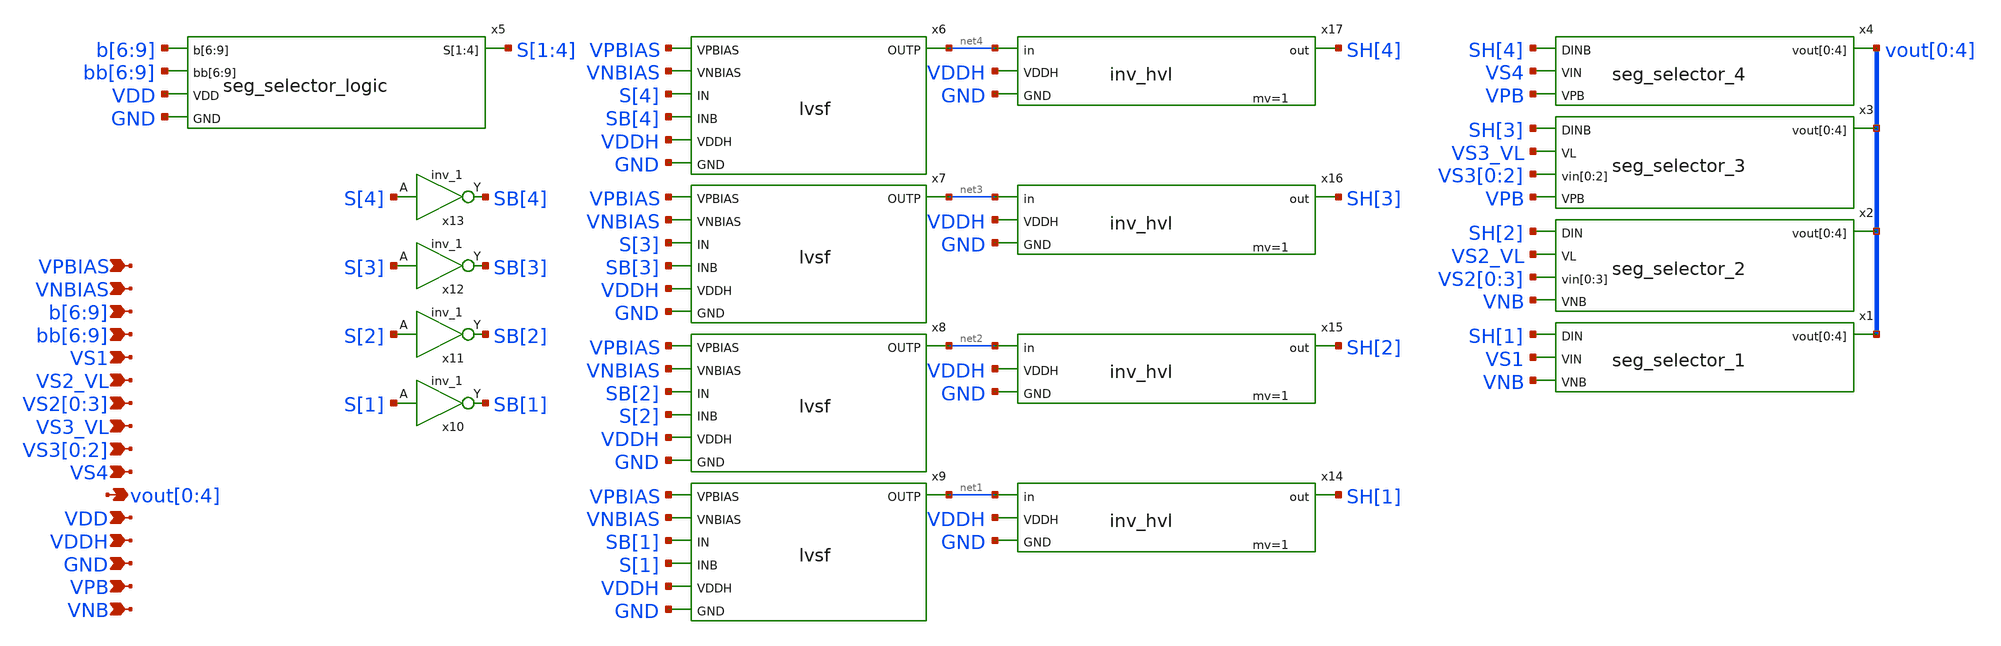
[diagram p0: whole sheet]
** sch_path: xschem/seg_selector.sch
**.subckt seg_selector vout[0],vout[1],vout[2],vout[3],vout[4] VNB VPB b[6],b[7],b[8],b[9] VS1
*+ VS2[0],VS2[1],VS2[2],VS2[3] VS3[0],VS3[1],VS3[2] VS4 bb[6],bb[7],bb[8],bb[9] GND VDD VPBIAS VNBIAS VDDH VS2_VL VS3_VL
*.opin vout[0],vout[1],vout[2],vout[3],vout[4]
*.ipin VNB
*.ipin VPB
*.ipin b[6],b[7],b[8],b[9]
*.ipin VS1
*.ipin VS2[0],VS2[1],VS2[2],VS2[3]
*.ipin VS3[0],VS3[1],VS3[2]
*.ipin VS4
*.ipin bb[6],bb[7],bb[8],bb[9]
*.ipin GND
*.ipin VDD
*.ipin VPBIAS
*.ipin VNBIAS
*.ipin VDDH
*.ipin VS2_VL
*.ipin VS3_VL
x1 SH[1] VS1 vout[0] vout[1] vout[2] vout[3] vout[4] VNB seg_selector_1
x2 SH[2] VS2_VL VS2[0] VS2[1] VS2[2] VS2[3] vout[0] vout[1] vout[2] vout[3] vout[4] VNB
+ seg_selector_2
x3 SH[3] VS3_VL VS3[0] VS3[1] VS3[2] vout[0] vout[1] vout[2] vout[3] vout[4] VPB seg_selector_3
x4 SH[4] VS4 vout[0] vout[1] vout[2] vout[3] vout[4] VPB seg_selector_4
x5 b[6] b[7] b[8] b[9] bb[6] bb[7] bb[8] bb[9] S[1] S[2] S[3] S[4] VDD GND seg_selector_logic
x6 VPBIAS VNBIAS S[4] SB[4] net4 VDDH GND lvsf
x7 VPBIAS VNBIAS S[3] SB[3] net3 VDDH GND lvsf
x8 VPBIAS VNBIAS SB[2] S[2] net2 VDDH GND lvsf
x9 VPBIAS VNBIAS SB[1] S[1] net1 VDDH GND lvsf
x10 S[1] GND GND VDD VDD SB[1] sky130_fd_sc_hd__inv_1
x11 S[2] GND GND VDD VDD SB[2] sky130_fd_sc_hd__inv_1
x12 S[3] GND GND VDD VDD SB[3] sky130_fd_sc_hd__inv_1
x13 S[4] GND GND VDD VDD SB[4] sky130_fd_sc_hd__inv_1
x14 net1 SH[1] VDDH GND inv_hvl mv=1
x15 net2 SH[2] VDDH GND inv_hvl mv=1
x16 net3 SH[3] VDDH GND inv_hvl mv=1
x17 net4 SH[4] VDDH GND inv_hvl mv=1
**.ends
.end
